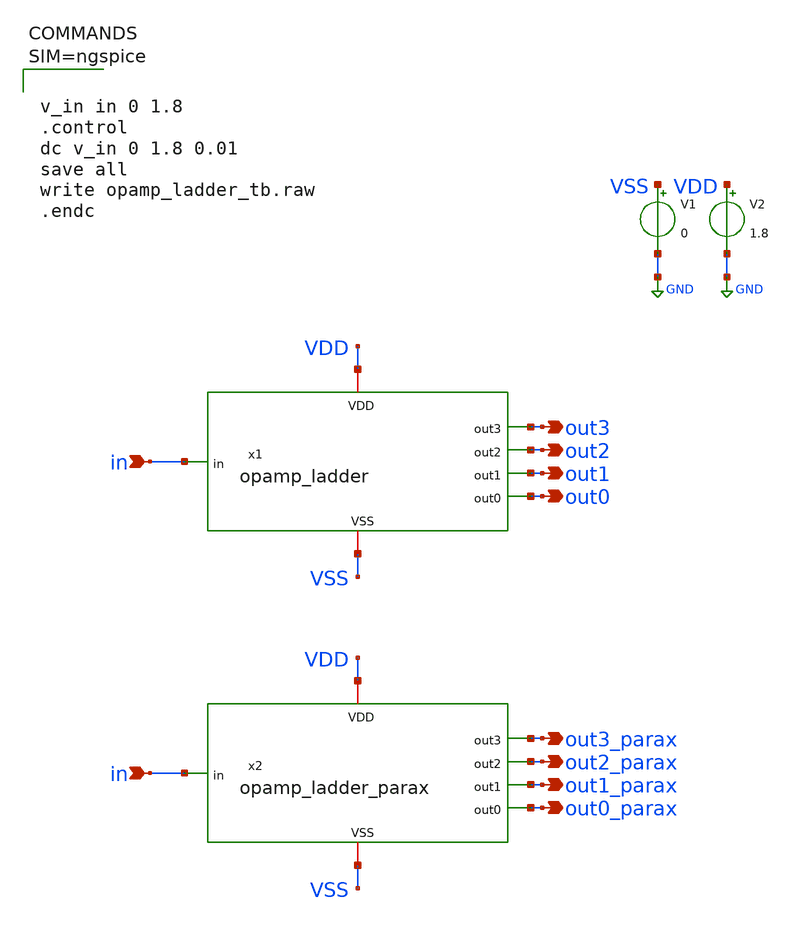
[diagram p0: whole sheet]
** sch_path: xschem/opamp_ladder_tb.sch
**.subckt opamp_ladder_tb out0 out1 out2 out3 in out0_parax out1_parax out2_parax out3_parax in
*.opin out0
*.opin out1
*.opin out2
*.opin out3
*.ipin in
*.opin out0_parax
*.opin out1_parax
*.opin out2_parax
*.opin out3_parax
*.ipin in
x1 VDD in VSS out3 out2 out1 out0 opamp_ladder
V1 VSS GND 0
V2 VDD GND 1.8
x2 VDD in VSS out3_parax out2_parax out1_parax out0_parax opamp_ladder_parax
**** begin user architecture code

** opencircuitdesign pdks install
.lib $::SKYWATER_MODELS/sky130.lib.spice tt





v_in in 0 1.8
.control
dc v_in 0 1.8 0.01
save all
write opamp_ladder_tb.raw
.endc



**** end user architecture code
**.ends

* expanding   symbol:  opamp_ladder.sym # of pins=7
** sym_path: xschem/opamp_ladder.sym
** sch_path: xschem/opamp_ladder.sch
.subckt opamp_ladder VDD in VSS out3 out2 out1 out0
*.opin out0
*.opin out2
*.opin out3
*.ipin in
*.iopin VDD
*.iopin VSS
*.opin out1
x1 VDD VSS node_0 in out0 VSS opamp
XR2 VSS node_0 VSS sky130_fd_pr__res_generic_nd W=1 L=8.4 mult=1 m=1
XR3 node_0 node_1 VSS sky130_fd_pr__res_generic_nd W=1 L=8.4 mult=1 m=1
XR4 node_1 node_2 VSS sky130_fd_pr__res_generic_nd W=1 L=8.4 mult=1 m=1
XR5 node_2 node_3 VSS sky130_fd_pr__res_generic_nd W=1 L=8.4 mult=1 m=1
x2 VDD VSS node_1 in out1 VSS opamp
x3 VDD VSS node_2 in out2 VSS opamp
x4 VDD VSS node_3 in out3 VSS opamp
XR1 node_3 VDD VSS sky130_fd_pr__res_generic_nd W=1 L=8.4 mult=1 m=1
.ends


* expanding   symbol:  opamp_ladder_parax.sym # of pins=7
** sym_path: xschem/opamp_ladder.sym
.include [file normalize ../mag/opamp_ladder.sim.spice]

* expanding   symbol:  opamp.sym # of pins=6
** sym_path: xschem/opamp.sym
** sch_path: xschem/opamp.sch
.subckt opamp VDD ZREF vin_n vin_p Vout VGND
*.ipin vin_n
*.ipin vin_p
*.opin Vout
*.iopin VDD
*.iopin ZREF
*.iopin VGND
XM1 net1 vin_n net3 net3 sky130_fd_pr__pfet_01v8 L=0.6 W=6 nf=1 ad='W * 0.29' as='W * 0.29' pd='2 * (W + 0.29)'
+ ps='2 * (W + 0.29)' nrd='0.29 / W' nrs='0.29 / W' sa=0 sb=0 sd=0 mult=1 m=1
XM2 net2 vin_p net3 net3 sky130_fd_pr__pfet_01v8 L=0.6 W=6 nf=1 ad='W * 0.29' as='W * 0.29' pd='2 * (W + 0.29)'
+ ps='2 * (W + 0.29)' nrd='0.29 / W' nrs='0.29 / W' sa=0 sb=0 sd=0 mult=1 m=1
XM3 net1 net1 VGND VGND sky130_fd_pr__nfet_01v8 L=0.6 W=6 nf=1 ad='W * 0.29' as='W * 0.29' pd='2 * (W + 0.29)'
+ ps='2 * (W + 0.29)' nrd='0.29 / W' nrs='0.29 / W' sa=0 sb=0 sd=0 mult=1 m=1
XM4 net2 net1 VGND VGND sky130_fd_pr__nfet_01v8 L=0.6 W=6 nf=1 ad='W * 0.29' as='W * 0.29' pd='2 * (W + 0.29)'
+ ps='2 * (W + 0.29)' nrd='0.29 / W' nrs='0.29 / W' sa=0 sb=0 sd=0 mult=1 m=1
XM5 net3 VGND VDD VDD sky130_fd_pr__pfet_01v8 L=0.6 W=6 nf=1 ad='W * 0.29' as='W * 0.29' pd='2 * (W + 0.29)'
+ ps='2 * (W + 0.29)' nrd='0.29 / W' nrs='0.29 / W' sa=0 sb=0 sd=0 mult=1 m=1
XM7 Vout VGND VDD VDD sky130_fd_pr__pfet_01v8 L=0.6 W=6 nf=1 ad='W * 0.29' as='W * 0.29' pd='2 * (W + 0.29)'
+ ps='2 * (W + 0.29)' nrd='0.29 / W' nrs='0.29 / W' sa=0 sb=0 sd=0 mult=1 m=1
XM8 ZREF VGND VDD VDD sky130_fd_pr__pfet_01v8 L=0.6 W=6 nf=1 ad='W * 0.29' as='W * 0.29' pd='2 * (W + 0.29)'
+ ps='2 * (W + 0.29)' nrd='0.29 / W' nrs='0.29 / W' sa=0 sb=0 sd=0 mult=1 m=1
XM9 net4 VDD net2 VGND sky130_fd_pr__nfet_01v8 L=0.6 W=1 nf=1 ad='W * 0.29' as='W * 0.29' pd='2 * (W + 0.29)'
+ ps='2 * (W + 0.29)' nrd='0.29 / W' nrs='0.29 / W' sa=0 sb=0 sd=0 mult=1 m=1
XC1 net4 Vout sky130_fd_pr__cap_mim_m3_1 W=17.55 L=15 MF=1 m=1
XM6 Vout net2 VGND VGND sky130_fd_pr__nfet_01v8 L=0.6 W=6 nf=1 ad='W * 0.29' as='W * 0.29' pd='2 * (W + 0.29)'
+ ps='2 * (W + 0.29)' nrd='0.29 / W' nrs='0.29 / W' sa=0 sb=0 sd=0 mult=1 m=1
XR1 ZREF VDD VGND sky130_fd_pr__res_generic_nd W=1 L=5 mult=1 m=1
XR2 VGND ZREF VGND sky130_fd_pr__res_generic_nd W=1 L=5 mult=1 m=1
.ends

.GLOBAL GND
.end
